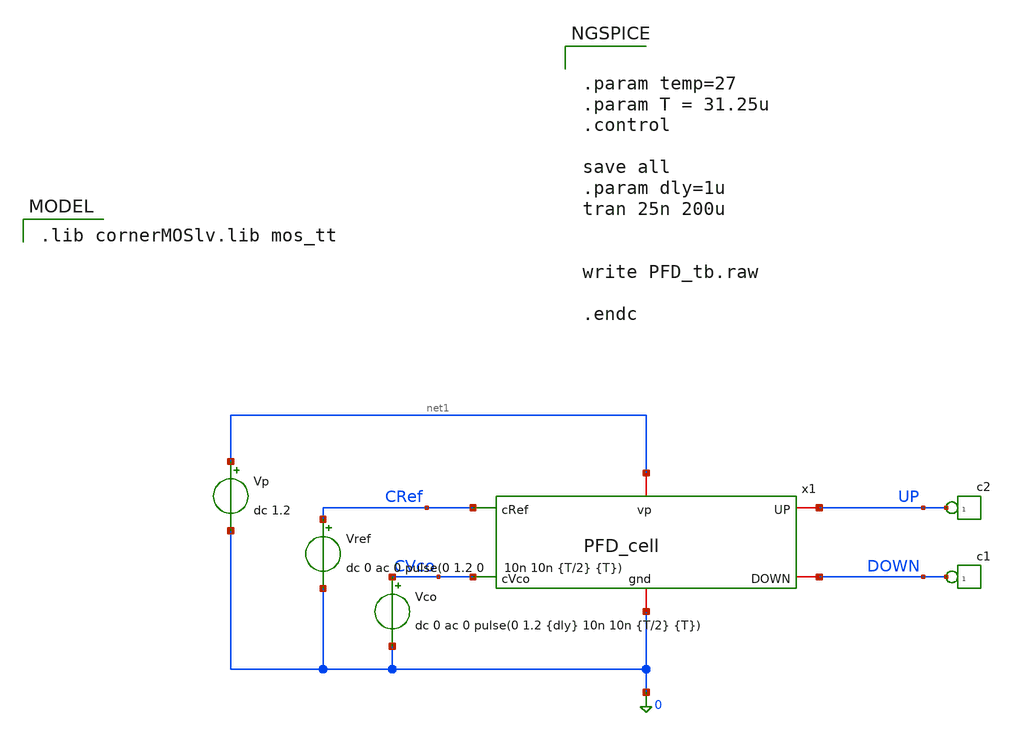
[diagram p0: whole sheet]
** sch_path: PFD/PFD_tb.sch
**.subckt PFD_tb
x1 0 net1 CRef UP DOWN CVco PFD_cell
*connector(1,1) ?1 DOWN
*connector(1,1) ?1 UP
Vref CRef 0 dc 0 ac 0 pulse(0 1.2 0 10n 10n {T/2} {T})
Vco CVco 0 dc 0 ac 0 pulse(0 1.2 {dly} 10n 10n {T/2} {T})
Vp net1 0 dc 1.2
**** begin user architecture code
 .lib cornerMOSlv.lib mos_tt



.param temp=27
.param T = 31.25u
.control

save all
.param dly=1u
tran 25n 200u


write PFD_tb.raw

.endc


**** end user architecture code
**.ends
.end
